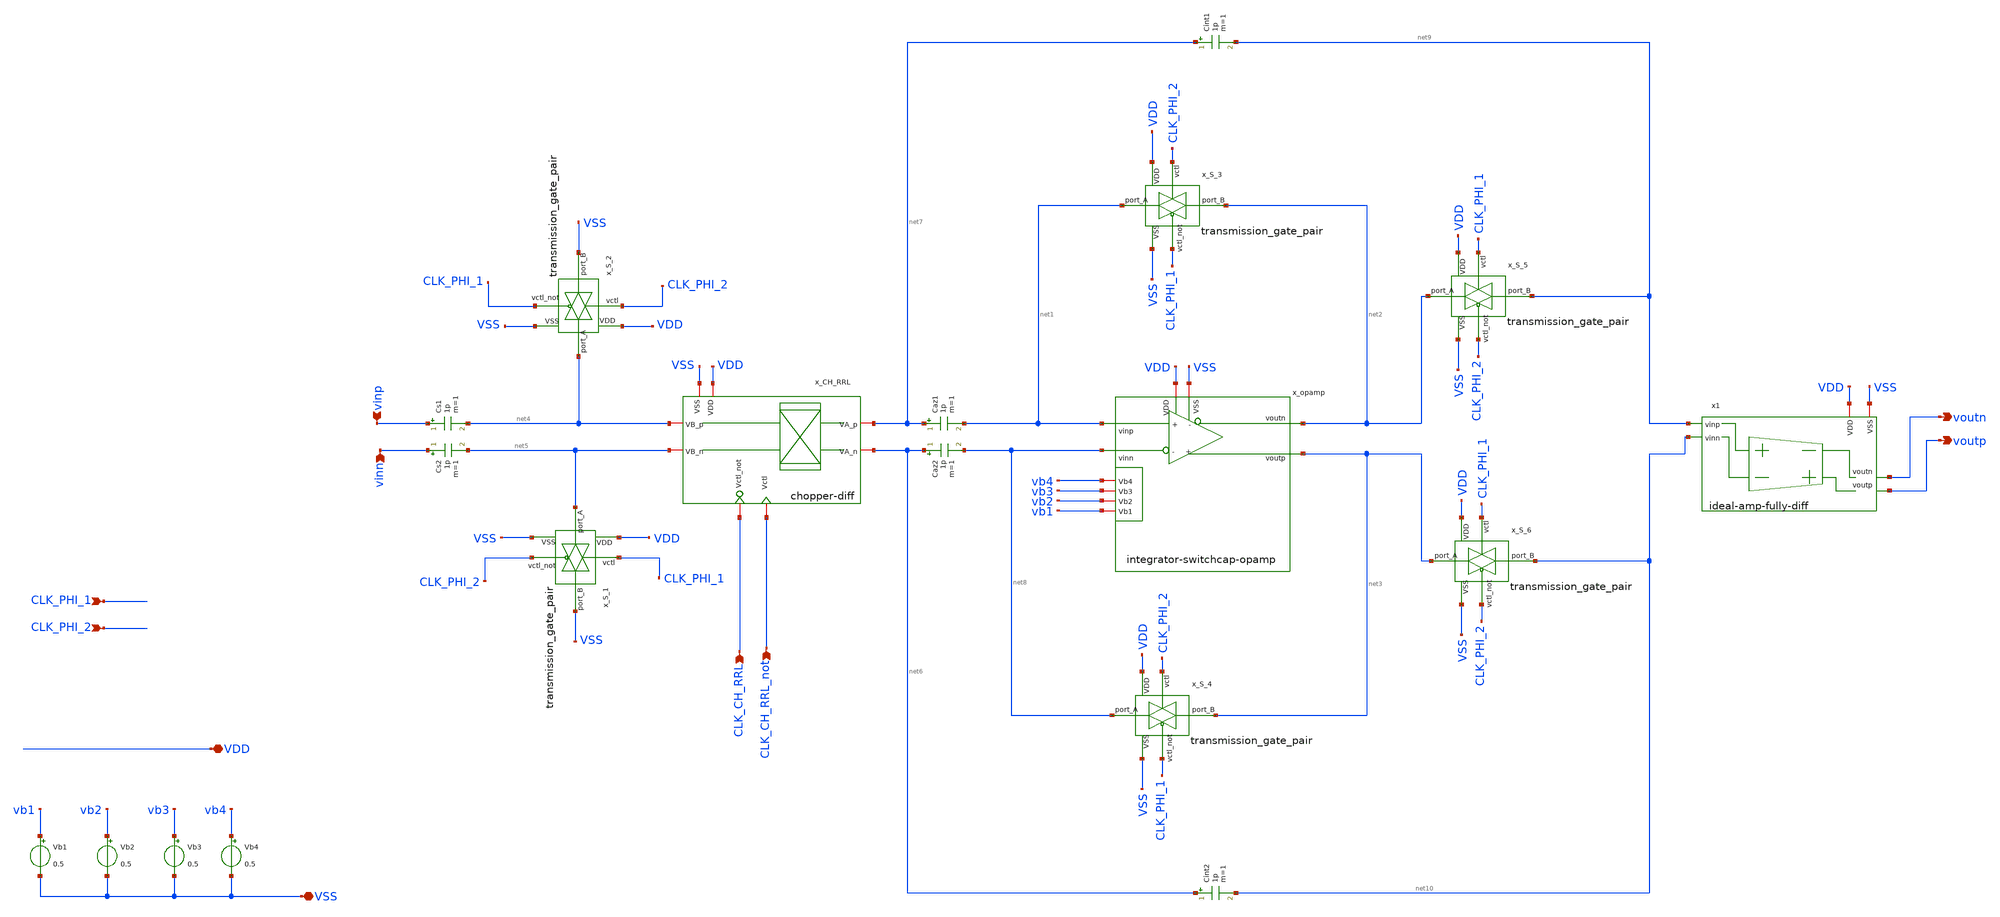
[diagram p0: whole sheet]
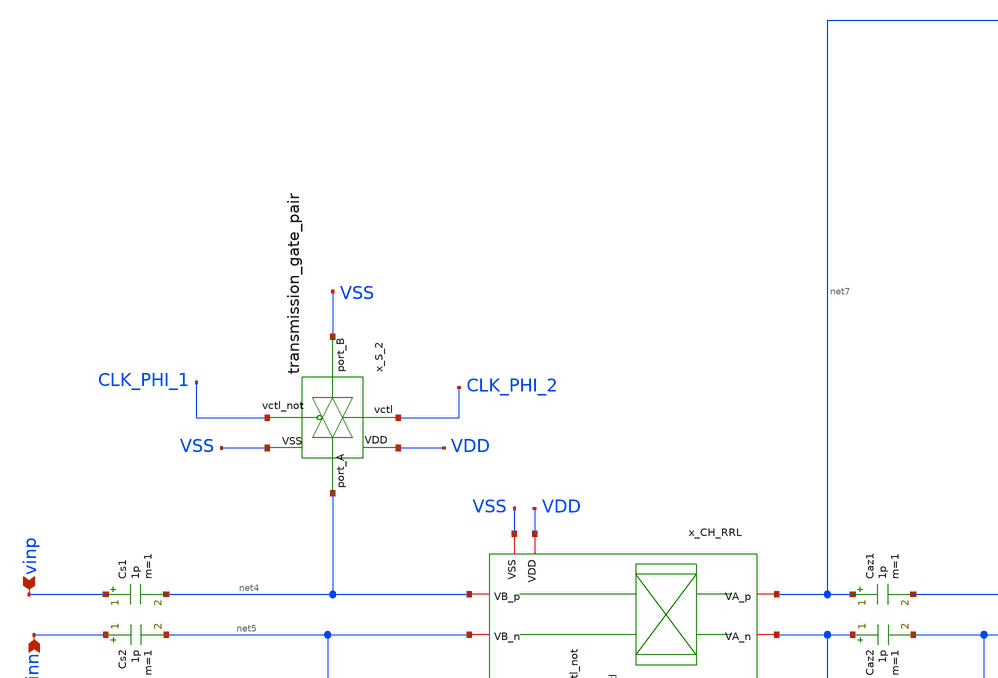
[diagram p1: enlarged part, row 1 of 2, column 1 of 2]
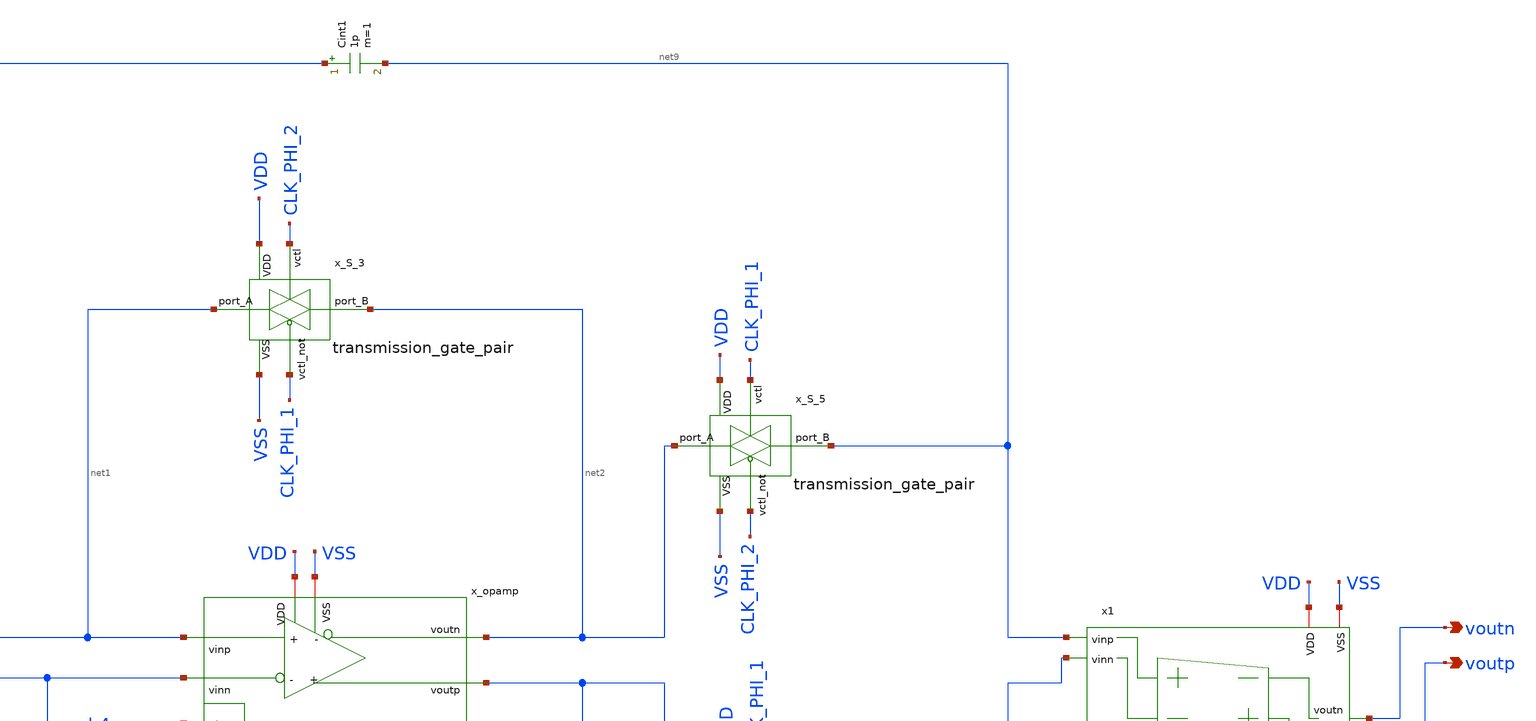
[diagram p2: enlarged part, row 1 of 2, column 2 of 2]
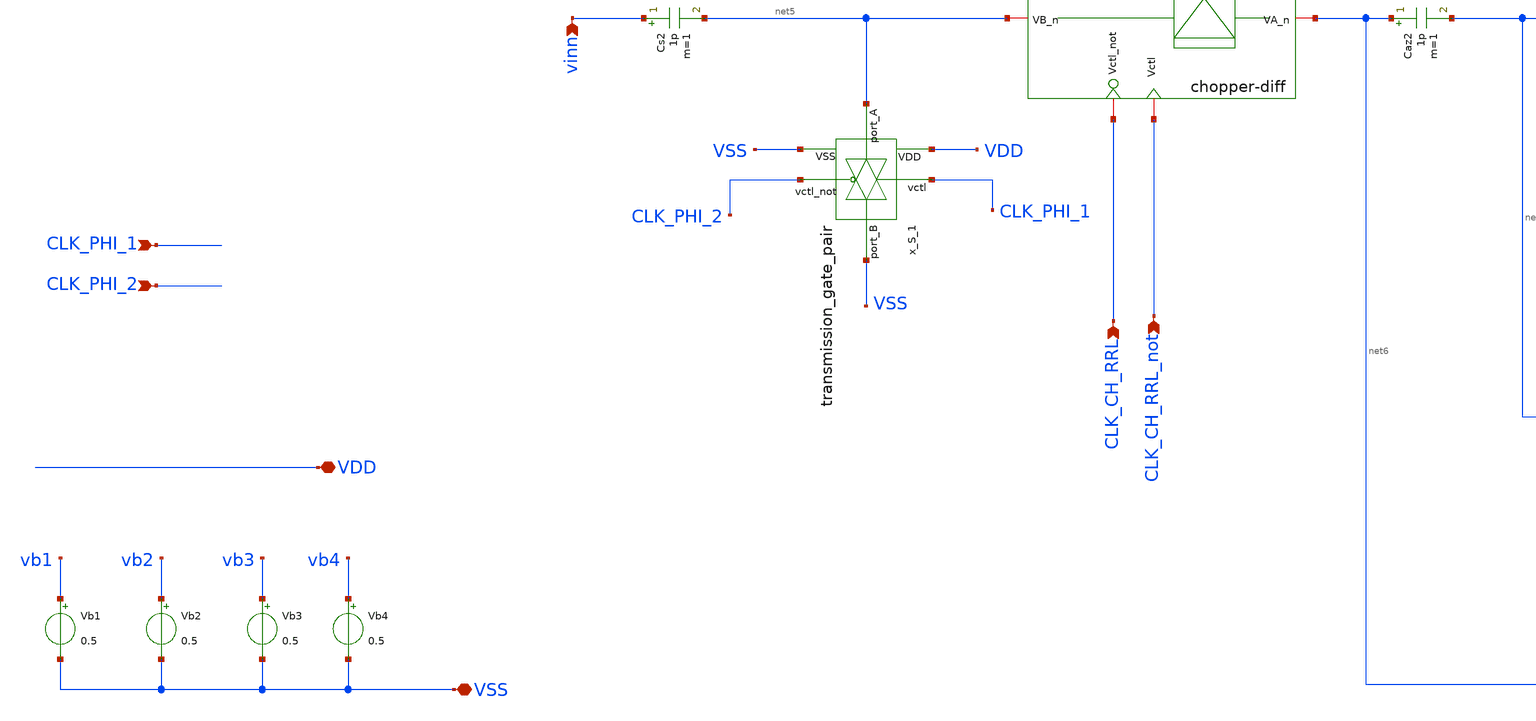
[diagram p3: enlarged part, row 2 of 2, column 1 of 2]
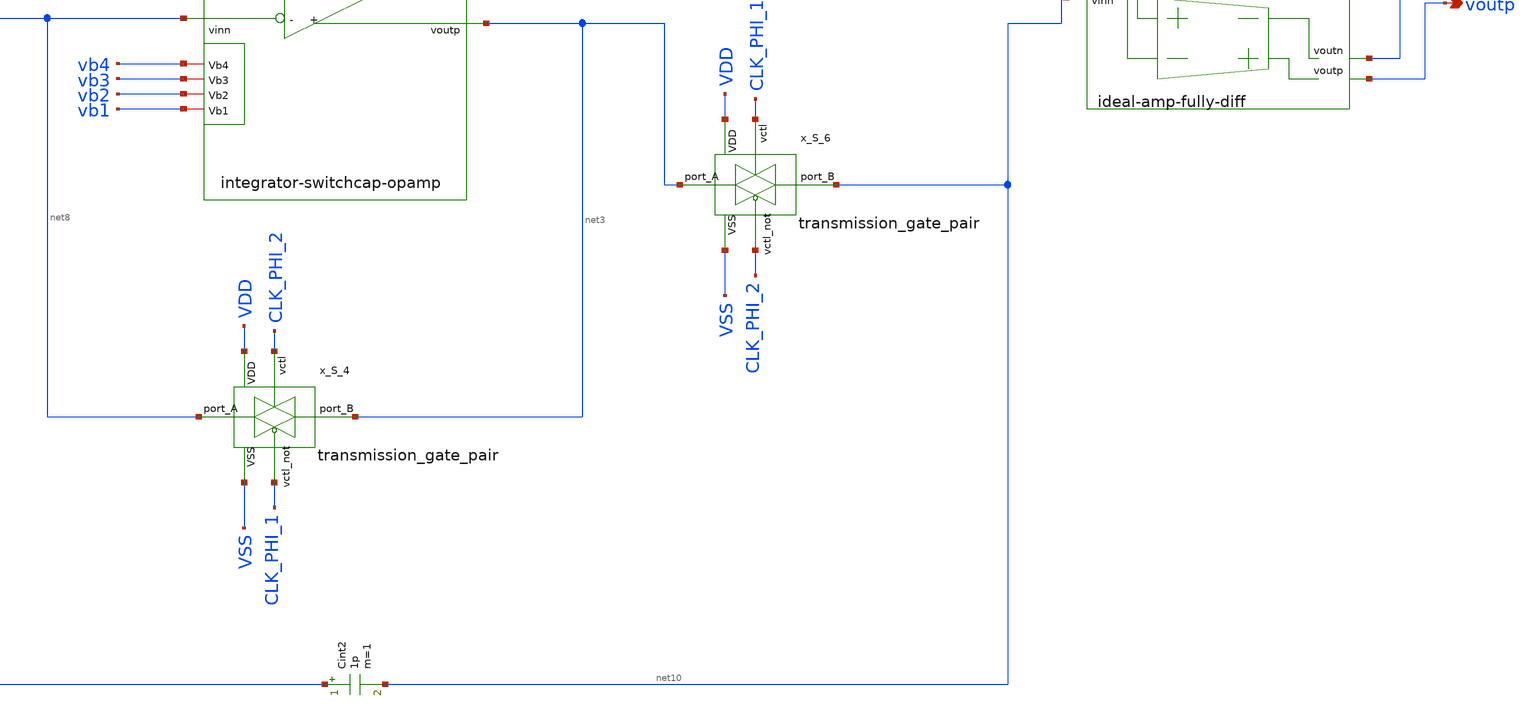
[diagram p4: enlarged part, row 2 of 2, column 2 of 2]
** sch_path: analog-db/circuits/sup_003_rrl_sc_integrator/pdk/ihp-sg13g2/schematic/rrl-switched-capa-integrator.sch
* Copyright 2026 MacAnalog Research Group
**.subckt rrl-switched-capa-integrator VSS VDD vinp vinn CLK_CH_RRL CLK_CH_RRL_not voutn voutp
*+ CLK_PHI_1 CLK_PHI_2
*.iopin VSS
*.iopin VDD
*.ipin vinp
*.ipin vinn
*.ipin CLK_CH_RRL
*.ipin CLK_CH_RRL_not
*.opin voutn
*.opin voutp
*.ipin CLK_PHI_1
*.ipin CLK_PHI_2
x_opamp VDD vb4 net8 net2 vb3 net1 vb2 net3 vb1 VSS integrator-switchcap-opamp
Vb1 vb1 VSS 0.5
Vb2 vb2 VSS 0.5
Vb3 vb3 VSS 0.5
Vb4 vb4 VSS 0.5
x_CH_RRL CLK_CH_RRL_not VDD net4 net7 CLK_CH_RRL VSS net5 net6 chopper-diff
x_S_2 CLK_PHI_1 VDD VSS VSS net4 CLK_PHI_2 transmission_gate_pair
x_S_1 CLK_PHI_2 VDD VSS VSS net5 CLK_PHI_1 transmission_gate_pair
Cs1 vinp net4 1p m=1
Cs2 vinn net5 1p m=1
Caz1 net7 net1 1p m=1
Caz2 net6 net8 1p m=1
x_S_3 CLK_PHI_1 VDD net2 VSS net1 CLK_PHI_2 transmission_gate_pair
x_S_4 CLK_PHI_1 VDD net3 VSS net8 CLK_PHI_2 transmission_gate_pair
x_S_5 CLK_PHI_2 VDD net9 VSS net2 CLK_PHI_1 transmission_gate_pair
x_S_6 CLK_PHI_2 VDD net10 VSS net3 CLK_PHI_1 transmission_gate_pair
Cint1 net7 net9 1p m=1
Cint2 net6 net10 1p m=1
x1 net9 net10 voutn voutp VSS VDD ideal-amp-fully-diff
**.ends
.end
